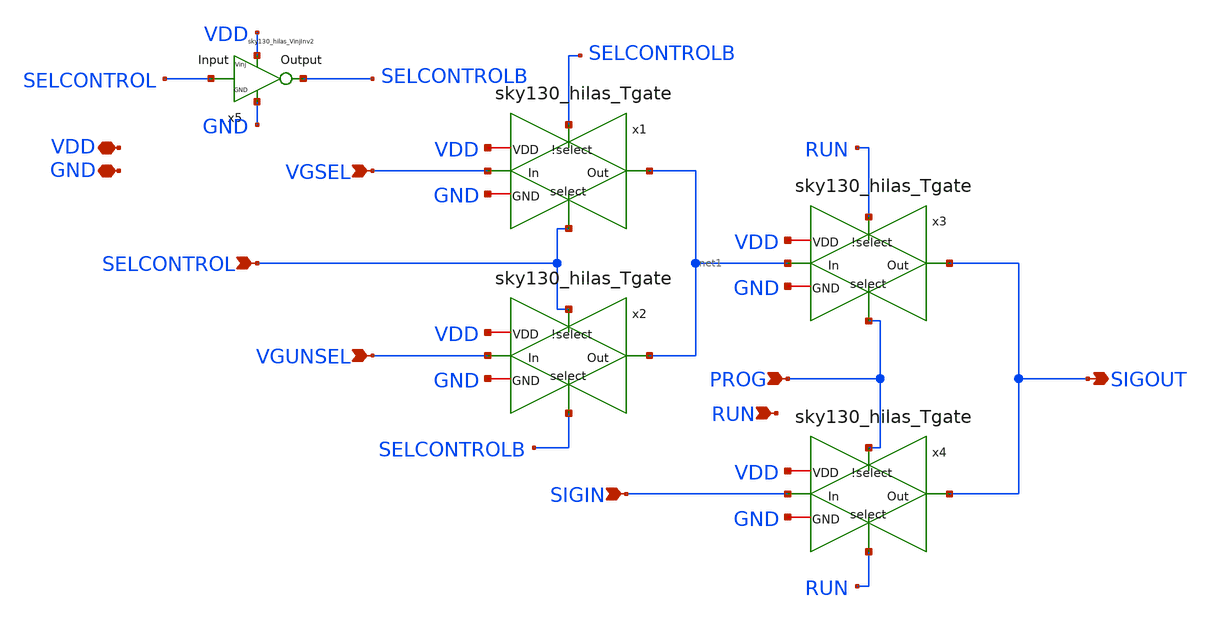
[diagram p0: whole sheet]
** sch_path: sky130_cells/Mux/Design/sky130_hilas_GateMuxSwc.sch
**.subckt sky130_hilas_GateMuxSwc SIGOUT SIGIN PROG RUN VDD GND VGUNSEL VGSEL SELCONTROL
*.opin SIGOUT
*.ipin SIGIN
*.ipin PROG
*.ipin RUN
*.iopin VDD
*.iopin GND
*.ipin VGUNSEL
*.ipin VGSEL
*.ipin SELCONTROL
x5 VDD SELCONTROL SELCONTROLB GND sky130_hilas_VinjInv2
x1 SELCONTROLB VDD net1 VGSEL GND SELCONTROL sky130_hilas_Tgate
x2 SELCONTROL VDD net1 VGUNSEL GND SELCONTROLB sky130_hilas_Tgate
x3 RUN VDD SIGOUT net1 GND PROG sky130_hilas_Tgate
x4 PROG VDD SIGOUT SIGIN GND RUN sky130_hilas_Tgate
**.ends

* expanding   symbol:  sky130_cells/RDAC/Design/sky130_hilas_VinjInv2.sym # of pins=4
** sym_path: sky130_cells/RDAC/Design/sky130_hilas_VinjInv2.sym
** sch_path: sky130_cells/RDAC/Design/sky130_hilas_VinjInv2.sch
.subckt sky130_hilas_VinjInv2 Vinj Input Output GND
*.ipin Input
*.opin Output
*.iopin Vinj
*.iopin GND
XM4 Output Input Vinj Vinj sky130_fd_pr__pfet_g5v0d10v5 L=0.53 W=0.42 nf=1 ad='int((nf+1)/2) * W/nf * 0.29'
+ as='int((nf+2)/2) * W/nf * 0.29' pd='2*int((nf+1)/2) * (W/nf + 0.29)' ps='2*int((nf+2)/2) * (W/nf + 0.29)'
+ nrd='0.29 / W' nrs='0.29 / W' sa=0 sb=0 sd=0 mult=1 m=1
XM3 Output Input GND GND sky130_fd_pr__nfet_g5v0d10v5 L=0.52 W=0.42 nf=1 ad='int((nf+1)/2) * W/nf * 0.29'
+ as='int((nf+2)/2) * W/nf * 0.29' pd='2*int((nf+1)/2) * (W/nf + 0.29)' ps='2*int((nf+2)/2) * (W/nf + 0.29)'
+ nrd='0.29 / W' nrs='0.29 / W' sa=0 sb=0 sd=0 mult=1 m=1
.ends


* expanding   symbol:  sky130_cells/Mux/Design/sky130_hilas_Tgate.sym # of pins=6
** sym_path: sky130_cells/Mux/Design/sky130_hilas_Tgate.sym
** sch_path: sky130_cells/Mux/Design/sky130_hilas_Tgate.sch
.subckt sky130_hilas_Tgate !select VDD Out In GND select
*.ipin In
*.ipin select
*.ipin !select
*.iopin VDD
*.iopin GND
*.opin Out
XM4 In select Out GND sky130_fd_pr__nfet_g5v0d10v5 L=0.5 W=2.25 nf=1 ad='int((nf+1)/2) * W/nf * 0.29'
+ as='int((nf+2)/2) * W/nf * 0.29' pd='2*int((nf+1)/2) * (W/nf + 0.29)' ps='2*int((nf+2)/2) * (W/nf + 0.29)'
+ nrd='0.29 / W' nrs='0.29 / W' sa=0 sb=0 sd=0 mult=1 m=1
XM2 In !select Out VDD sky130_fd_pr__pfet_g5v0d10v5 L=0.5 W=2.25 nf=1 ad='int((nf+1)/2) * W/nf * 0.29'
+ as='int((nf+2)/2) * W/nf * 0.29' pd='2*int((nf+1)/2) * (W/nf + 0.29)' ps='2*int((nf+2)/2) * (W/nf + 0.29)'
+ nrd='0.29 / W' nrs='0.29 / W' sa=0 sb=0 sd=0 mult=1 m=1
XM5 In select Out GND sky130_fd_pr__nfet_g5v0d10v5 L=0.5 W=2.25 nf=1 ad='int((nf+1)/2) * W/nf * 0.29'
+ as='int((nf+2)/2) * W/nf * 0.29' pd='2*int((nf+1)/2) * (W/nf + 0.29)' ps='2*int((nf+2)/2) * (W/nf + 0.29)'
+ nrd='0.29 / W' nrs='0.29 / W' sa=0 sb=0 sd=0 mult=1 m=1
XM6 In !select Out VDD sky130_fd_pr__pfet_g5v0d10v5 L=0.5 W=2.25 nf=1 ad='int((nf+1)/2) * W/nf * 0.29'
+ as='int((nf+2)/2) * W/nf * 0.29' pd='2*int((nf+1)/2) * (W/nf + 0.29)' ps='2*int((nf+2)/2) * (W/nf + 0.29)'
+ nrd='0.29 / W' nrs='0.29 / W' sa=0 sb=0 sd=0 mult=1 m=1
.ends

.end
